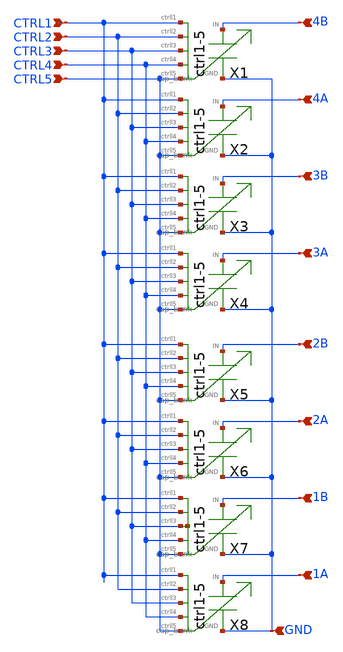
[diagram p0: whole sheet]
** sch_path: design/vco/100M~5G/cap_bank8.sch
**.subckt cap_bank8 CTRL1 CTRL2 CTRL3 CTRL4 CTRL5 GND 4B 4A 3B 3A 2B 2A 1B 1A
*.ipin CTRL1
*.ipin CTRL2
*.ipin CTRL3
*.ipin CTRL4
*.ipin CTRL5
*.ipin GND
*.ipin 4B
*.ipin 4A
*.ipin 3B
*.ipin 3A
*.ipin 2B
*.ipin 2A
*.ipin 1B
*.ipin 1A
X1 4B GND CTRL1 CTRL2 CTRL3 CTRL4 CTRL5 cap_bank
X2 4A GND CTRL1 CTRL2 CTRL3 CTRL4 CTRL5 cap_bank
X3 3B GND CTRL1 CTRL2 CTRL3 CTRL4 CTRL5 cap_bank
X4 3A GND CTRL1 CTRL2 CTRL3 CTRL4 CTRL5 cap_bank
X5 2B GND CTRL1 CTRL2 CTRL3 CTRL4 CTRL5 cap_bank
X6 2A GND CTRL1 CTRL2 CTRL3 CTRL4 CTRL5 cap_bank
X7 1B GND CTRL1 CTRL2 CTRL3 CTRL4 CTRL5 cap_bank
X8 1A GND CTRL1 CTRL2 CTRL3 CTRL4 CTRL5 cap_bank
**.ends

* expanding   symbol:  cap_bank.sym # of pins=7
** sym_path: design/vco/1.7G~10G/schematic/cap_bank.sym
** sch_path: design/vco/1.7G~10G/schematic/cap_bank.sch
.subckt cap_bank IN GND ctrll1 ctrll2 ctrll3 ctrll4 ctrll5
*.ipin IN
*.ipin GND
*.ipin ctrll1
*.ipin ctrll2
*.ipin ctrll3
*.ipin ctrll4
*.ipin ctrll5
XC6 IN net1 sky130_fd_pr__cap_mim_m3_2 W=2 L=2 MF=1 m=1
XC1 IN net5 sky130_fd_pr__cap_mim_m3_2 W=2 L=2 MF=1 m=1
XC2 IN net4 sky130_fd_pr__cap_mim_m3_2 W=3 L=2 MF=1 m=1
XC3 IN net3 sky130_fd_pr__cap_mim_m3_2 W=3 L=4 MF=1 m=1
XC4 IN net2 sky130_fd_pr__cap_mim_m3_2 W=6 L=4 MF=1 m=1
XM1 net1 ctrll1 GND GND sky130_fd_pr__nfet_01v8_lvt L=0.15 W=1 nf=1 ad='int((nf+1)/2) * W/nf * 0.29'
+ as='int((nf+2)/2) * W/nf * 0.29' pd='2*int((nf+1)/2) * (W/nf + 0.29)' ps='2*int((nf+2)/2) * (W/nf + 0.29)'
+ nrd='0.29 / W' nrs='0.29 / W' sa=0 sb=0 sd=0 mult=1 m=1
XM2 net5 ctrll2 GND GND sky130_fd_pr__nfet_01v8_lvt L=0.15 W=1 nf=1 ad='int((nf+1)/2) * W/nf * 0.29'
+ as='int((nf+2)/2) * W/nf * 0.29' pd='2*int((nf+1)/2) * (W/nf + 0.29)' ps='2*int((nf+2)/2) * (W/nf + 0.29)'
+ nrd='0.29 / W' nrs='0.29 / W' sa=0 sb=0 sd=0 mult=1 m=1
XM3 net4 ctrll3 GND GND sky130_fd_pr__nfet_01v8_lvt L=0.15 W=2 nf=2 ad='int((nf+1)/2) * W/nf * 0.29'
+ as='int((nf+2)/2) * W/nf * 0.29' pd='2*int((nf+1)/2) * (W/nf + 0.29)' ps='2*int((nf+2)/2) * (W/nf + 0.29)'
+ nrd='0.29 / W' nrs='0.29 / W' sa=0 sb=0 sd=0 mult=1 m=1
XM4 net3 ctrll4 GND GND sky130_fd_pr__nfet_01v8_lvt L=0.15 W=3 nf=3 ad='int((nf+1)/2) * W/nf * 0.29'
+ as='int((nf+2)/2) * W/nf * 0.29' pd='2*int((nf+1)/2) * (W/nf + 0.29)' ps='2*int((nf+2)/2) * (W/nf + 0.29)'
+ nrd='0.29 / W' nrs='0.29 / W' sa=0 sb=0 sd=0 mult=1 m=1
XM5 net2 ctrll5 GND GND sky130_fd_pr__nfet_01v8_lvt L=0.15 W=6 nf=6 ad='int((nf+1)/2) * W/nf * 0.29'
+ as='int((nf+2)/2) * W/nf * 0.29' pd='2*int((nf+1)/2) * (W/nf + 0.29)' ps='2*int((nf+2)/2) * (W/nf + 0.29)'
+ nrd='0.29 / W' nrs='0.29 / W' sa=0 sb=0 sd=0 mult=1 m=1
.ends

.end
